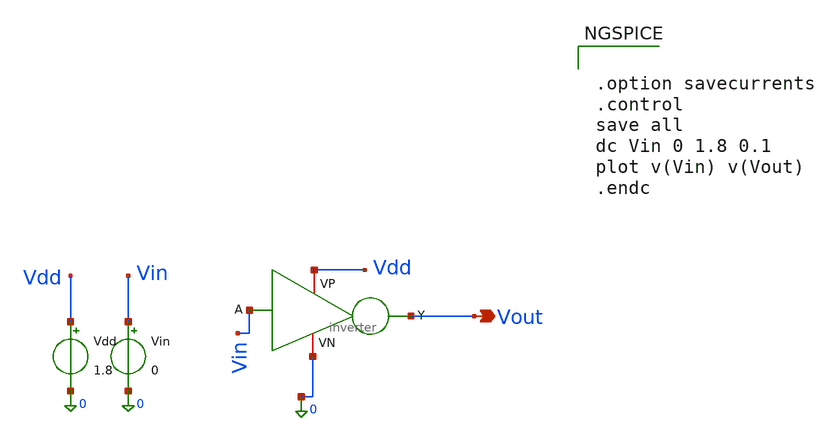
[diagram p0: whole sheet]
** sch_path: Familiarization of open source design flow/Testbench/inverter_dc_tb.sch
**.subckt inverter_dc_tb Vout
*.opin Vout
Vdd Vdd 0 1.8
Vin Vin 0 0
x1 Vdd Vin Vout 0 inverter
**** begin user architecture code

** opencircuitdesign pdks install
.lib $::SKYWATER_MODELS/sky130.lib.spice tt



.option savecurrents
.control
save all
dc Vin 0 1.8 0.1
plot v(Vin) v(Vout)
.endc


**** end user architecture code
**.ends
.end
